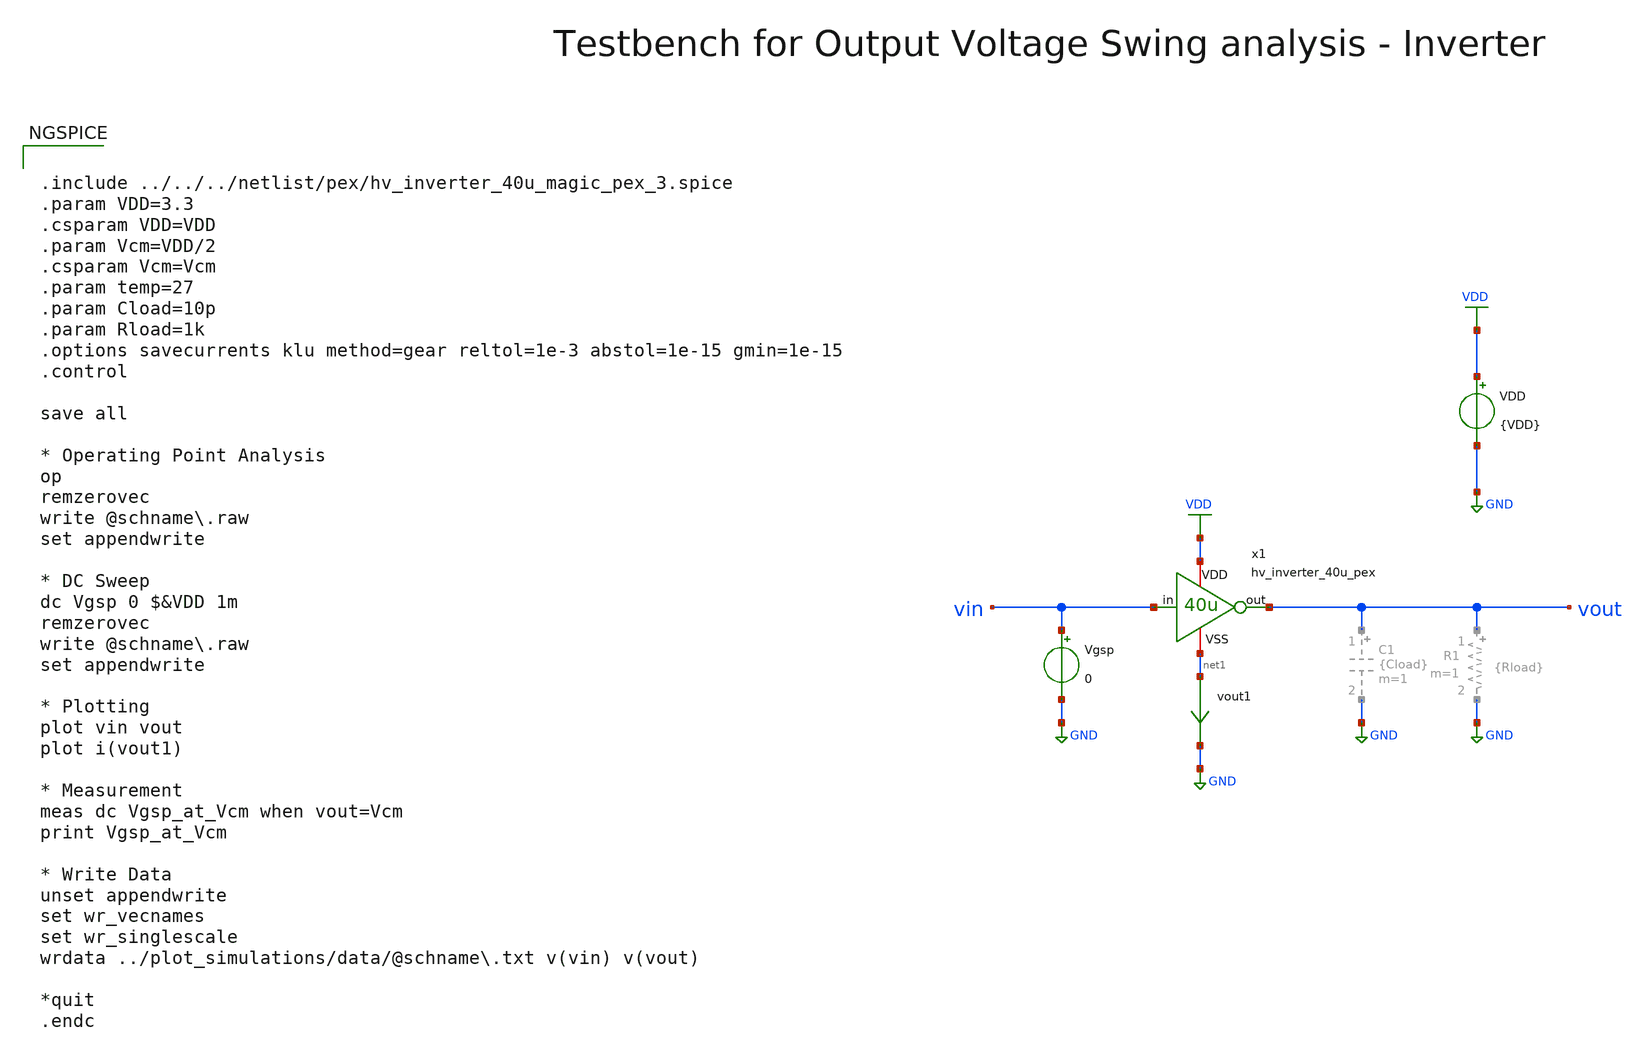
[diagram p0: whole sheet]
** sch_path: macros/heichips26_vcr/macros/switched_capacitor/testbenches/xschem/tb_hv_inverter_40u_pex_dc.sch
**.subckt tb_hv_inverter_40u_pex_dc
VDD VDD GND {VDD}
Vgsp vin GND 0
vout1 net1 GND 0
.save i(vout1)
x1 VDD vin vout net1 hv_inverter_40u_pex
**** begin user architecture code


.include ../../../netlist/pex/hv_inverter_40u_magic_pex_3.spice
.param VDD=3.3
.csparam VDD=VDD
.param Vcm=VDD/2
.csparam Vcm=Vcm
.param temp=27
.param Cload=10p
.param Rload=1k
.options savecurrents klu method=gear reltol=1e-3 abstol=1e-15 gmin=1e-15
.control

save all

* Operating Point Analysis
op
remzerovec
write @schname\.raw
set appendwrite

* DC Sweep
dc Vgsp 0 $&VDD 1m
remzerovec
write @schname\.raw
set appendwrite

* Plotting
plot vin vout
plot i(vout1)

* Measurement
meas dc Vgsp_at_Vcm when vout=Vcm
print Vgsp_at_Vcm

* Write Data
unset appendwrite
set wr_vecnames
set wr_singlescale
wrdata ../plot_simulations/data/@schname\.txt v(vin) v(vout)

*quit
.endc



.lib cornerMOSlv.lib mos_tt
.lib cornerMOShv.lib mos_tt
.lib cornerRES.lib res_typ
.lib cornerDIO.lib dio_tt

**** end user architecture code
**.ends
.GLOBAL GND
.GLOBAL VDD
.end
